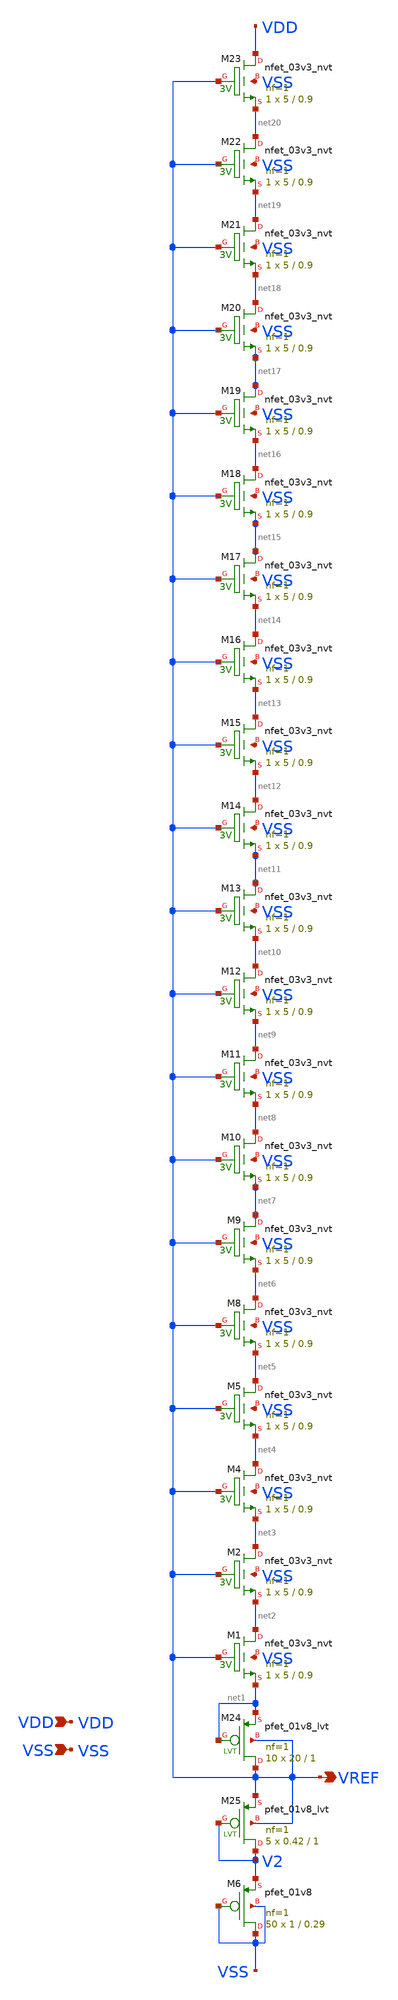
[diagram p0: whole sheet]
** sch_path: design/LELO_SVOD_SKY130A/LELO_SVOD_VTREF.sch
**.subckt LELO_SVOD_VTREF VDD VSS VREF
*.ipin VDD
*.ipin VSS
*.opin VREF
XM1 net2 VREF net1 VSS sky130_fd_pr__nfet_03v3_nvt L=0.9 W=5 nf=1 ad='int((1 + 1)/2) * 5 / 1 * 0.29'
+ as='int((1 + 2)/2) * 5 / 1 * 0.29' pd='2*int((1 + 1)/2) * (5 / 1 + 0.29)' ps='2*int((1 + 2)/2) * (5 / 1 + 0.29)'
+ nrd='0.29 / 5 ' nrs='0.29 / 5 ' sa=0 sb=0 sd=0 mult=1 m=1
XM2 net3 VREF net2 VSS sky130_fd_pr__nfet_03v3_nvt L=0.9 W=5 nf=1 ad='int((1 + 1)/2) * 5 / 1 * 0.29'
+ as='int((1 + 2)/2) * 5 / 1 * 0.29' pd='2*int((1 + 1)/2) * (5 / 1 + 0.29)' ps='2*int((1 + 2)/2) * (5 / 1 + 0.29)'
+ nrd='0.29 / 5 ' nrs='0.29 / 5 ' sa=0 sb=0 sd=0 mult=1 m=1
XM4 net4 VREF net3 VSS sky130_fd_pr__nfet_03v3_nvt L=0.9 W=5 nf=1 ad='int((1 + 1)/2) * 5 / 1 * 0.29'
+ as='int((1 + 2)/2) * 5 / 1 * 0.29' pd='2*int((1 + 1)/2) * (5 / 1 + 0.29)' ps='2*int((1 + 2)/2) * (5 / 1 + 0.29)'
+ nrd='0.29 / 5 ' nrs='0.29 / 5 ' sa=0 sb=0 sd=0 mult=1 m=1
XM5 net5 VREF net4 VSS sky130_fd_pr__nfet_03v3_nvt L=0.9 W=5 nf=1 ad='int((1 + 1)/2) * 5 / 1 * 0.29'
+ as='int((1 + 2)/2) * 5 / 1 * 0.29' pd='2*int((1 + 1)/2) * (5 / 1 + 0.29)' ps='2*int((1 + 2)/2) * (5 / 1 + 0.29)'
+ nrd='0.29 / 5 ' nrs='0.29 / 5 ' sa=0 sb=0 sd=0 mult=1 m=1
XM6 VSS VSS V2 VSS sky130_fd_pr__pfet_01v8 L=0.29 W=1 nf=1 ad='int((1 + 1)/2) * 1 / 1 * 0.29' as='int((1 + 2)/2) * 1 / 1 * 0.29'
+ pd='2*int((1 + 1)/2) * (1 / 1 + 0.29)' ps='2*int((1 + 2)/2) * (1 / 1 + 0.29)' nrd='0.29 / 1 ' nrs='0.29 / 1 '
+ sa=0 sb=0 sd=0 mult=50 m=50
XM8 net6 VREF net5 VSS sky130_fd_pr__nfet_03v3_nvt L=0.9 W=5 nf=1 ad='int((1 + 1)/2) * 5 / 1 * 0.29'
+ as='int((1 + 2)/2) * 5 / 1 * 0.29' pd='2*int((1 + 1)/2) * (5 / 1 + 0.29)' ps='2*int((1 + 2)/2) * (5 / 1 + 0.29)'
+ nrd='0.29 / 5 ' nrs='0.29 / 5 ' sa=0 sb=0 sd=0 mult=1 m=1
XM9 net7 VREF net6 VSS sky130_fd_pr__nfet_03v3_nvt L=0.9 W=5 nf=1 ad='int((1 + 1)/2) * 5 / 1 * 0.29'
+ as='int((1 + 2)/2) * 5 / 1 * 0.29' pd='2*int((1 + 1)/2) * (5 / 1 + 0.29)' ps='2*int((1 + 2)/2) * (5 / 1 + 0.29)'
+ nrd='0.29 / 5 ' nrs='0.29 / 5 ' sa=0 sb=0 sd=0 mult=1 m=1
XM10 net8 VREF net7 VSS sky130_fd_pr__nfet_03v3_nvt L=0.9 W=5 nf=1 ad='int((1 + 1)/2) * 5 / 1 * 0.29'
+ as='int((1 + 2)/2) * 5 / 1 * 0.29' pd='2*int((1 + 1)/2) * (5 / 1 + 0.29)' ps='2*int((1 + 2)/2) * (5 / 1 + 0.29)'
+ nrd='0.29 / 5 ' nrs='0.29 / 5 ' sa=0 sb=0 sd=0 mult=1 m=1
XM11 net9 VREF net8 VSS sky130_fd_pr__nfet_03v3_nvt L=0.9 W=5 nf=1 ad='int((1 + 1)/2) * 5 / 1 * 0.29'
+ as='int((1 + 2)/2) * 5 / 1 * 0.29' pd='2*int((1 + 1)/2) * (5 / 1 + 0.29)' ps='2*int((1 + 2)/2) * (5 / 1 + 0.29)'
+ nrd='0.29 / 5 ' nrs='0.29 / 5 ' sa=0 sb=0 sd=0 mult=1 m=1
XM12 net10 VREF net9 VSS sky130_fd_pr__nfet_03v3_nvt L=0.9 W=5 nf=1 ad='int((1 + 1)/2) * 5 / 1 * 0.29'
+ as='int((1 + 2)/2) * 5 / 1 * 0.29' pd='2*int((1 + 1)/2) * (5 / 1 + 0.29)' ps='2*int((1 + 2)/2) * (5 / 1 + 0.29)'
+ nrd='0.29 / 5 ' nrs='0.29 / 5 ' sa=0 sb=0 sd=0 mult=1 m=1
XM13 net11 VREF net10 VSS sky130_fd_pr__nfet_03v3_nvt L=0.9 W=5 nf=1 ad='int((1 + 1)/2) * 5 / 1 * 0.29'
+ as='int((1 + 2)/2) * 5 / 1 * 0.29' pd='2*int((1 + 1)/2) * (5 / 1 + 0.29)' ps='2*int((1 + 2)/2) * (5 / 1 + 0.29)'
+ nrd='0.29 / 5 ' nrs='0.29 / 5 ' sa=0 sb=0 sd=0 mult=1 m=1
XM14 net12 VREF net11 VSS sky130_fd_pr__nfet_03v3_nvt L=0.9 W=5 nf=1 ad='int((1 + 1)/2) * 5 / 1 * 0.29'
+ as='int((1 + 2)/2) * 5 / 1 * 0.29' pd='2*int((1 + 1)/2) * (5 / 1 + 0.29)' ps='2*int((1 + 2)/2) * (5 / 1 + 0.29)'
+ nrd='0.29 / 5 ' nrs='0.29 / 5 ' sa=0 sb=0 sd=0 mult=1 m=1
XM15 net13 VREF net12 VSS sky130_fd_pr__nfet_03v3_nvt L=0.9 W=5 nf=1 ad='int((1 + 1)/2) * 5 / 1 * 0.29'
+ as='int((1 + 2)/2) * 5 / 1 * 0.29' pd='2*int((1 + 1)/2) * (5 / 1 + 0.29)' ps='2*int((1 + 2)/2) * (5 / 1 + 0.29)'
+ nrd='0.29 / 5 ' nrs='0.29 / 5 ' sa=0 sb=0 sd=0 mult=1 m=1
XM16 net14 VREF net13 VSS sky130_fd_pr__nfet_03v3_nvt L=0.9 W=5 nf=1 ad='int((1 + 1)/2) * 5 / 1 * 0.29'
+ as='int((1 + 2)/2) * 5 / 1 * 0.29' pd='2*int((1 + 1)/2) * (5 / 1 + 0.29)' ps='2*int((1 + 2)/2) * (5 / 1 + 0.29)'
+ nrd='0.29 / 5 ' nrs='0.29 / 5 ' sa=0 sb=0 sd=0 mult=1 m=1
XM17 net15 VREF net14 VSS sky130_fd_pr__nfet_03v3_nvt L=0.9 W=5 nf=1 ad='int((1 + 1)/2) * 5 / 1 * 0.29'
+ as='int((1 + 2)/2) * 5 / 1 * 0.29' pd='2*int((1 + 1)/2) * (5 / 1 + 0.29)' ps='2*int((1 + 2)/2) * (5 / 1 + 0.29)'
+ nrd='0.29 / 5 ' nrs='0.29 / 5 ' sa=0 sb=0 sd=0 mult=1 m=1
XM18 net16 VREF net15 VSS sky130_fd_pr__nfet_03v3_nvt L=0.9 W=5 nf=1 ad='int((1 + 1)/2) * 5 / 1 * 0.29'
+ as='int((1 + 2)/2) * 5 / 1 * 0.29' pd='2*int((1 + 1)/2) * (5 / 1 + 0.29)' ps='2*int((1 + 2)/2) * (5 / 1 + 0.29)'
+ nrd='0.29 / 5 ' nrs='0.29 / 5 ' sa=0 sb=0 sd=0 mult=1 m=1
XM19 net17 VREF net16 VSS sky130_fd_pr__nfet_03v3_nvt L=0.9 W=5 nf=1 ad='int((1 + 1)/2) * 5 / 1 * 0.29'
+ as='int((1 + 2)/2) * 5 / 1 * 0.29' pd='2*int((1 + 1)/2) * (5 / 1 + 0.29)' ps='2*int((1 + 2)/2) * (5 / 1 + 0.29)'
+ nrd='0.29 / 5 ' nrs='0.29 / 5 ' sa=0 sb=0 sd=0 mult=1 m=1
XM20 net18 VREF net17 VSS sky130_fd_pr__nfet_03v3_nvt L=0.9 W=5 nf=1 ad='int((1 + 1)/2) * 5 / 1 * 0.29'
+ as='int((1 + 2)/2) * 5 / 1 * 0.29' pd='2*int((1 + 1)/2) * (5 / 1 + 0.29)' ps='2*int((1 + 2)/2) * (5 / 1 + 0.29)'
+ nrd='0.29 / 5 ' nrs='0.29 / 5 ' sa=0 sb=0 sd=0 mult=1 m=1
XM21 net19 VREF net18 VSS sky130_fd_pr__nfet_03v3_nvt L=0.9 W=5 nf=1 ad='int((1 + 1)/2) * 5 / 1 * 0.29'
+ as='int((1 + 2)/2) * 5 / 1 * 0.29' pd='2*int((1 + 1)/2) * (5 / 1 + 0.29)' ps='2*int((1 + 2)/2) * (5 / 1 + 0.29)'
+ nrd='0.29 / 5 ' nrs='0.29 / 5 ' sa=0 sb=0 sd=0 mult=1 m=1
XM22 net20 VREF net19 VSS sky130_fd_pr__nfet_03v3_nvt L=0.9 W=5 nf=1 ad='int((1 + 1)/2) * 5 / 1 * 0.29'
+ as='int((1 + 2)/2) * 5 / 1 * 0.29' pd='2*int((1 + 1)/2) * (5 / 1 + 0.29)' ps='2*int((1 + 2)/2) * (5 / 1 + 0.29)'
+ nrd='0.29 / 5 ' nrs='0.29 / 5 ' sa=0 sb=0 sd=0 mult=1 m=1
XM23 VDD VREF net20 VSS sky130_fd_pr__nfet_03v3_nvt L=0.9 W=5 nf=1 ad='int((1 + 1)/2) * 5 / 1 * 0.29'
+ as='int((1 + 2)/2) * 5 / 1 * 0.29' pd='2*int((1 + 1)/2) * (5 / 1 + 0.29)' ps='2*int((1 + 2)/2) * (5 / 1 + 0.29)'
+ nrd='0.29 / 5 ' nrs='0.29 / 5 ' sa=0 sb=0 sd=0 mult=1 m=1
XM24 VREF net1 net1 VREF sky130_fd_pr__pfet_01v8_lvt L=1 W=20 nf=1 ad='int((1 + 1)/2) * 20 / 1 * 0.29'
+ as='int((1 + 2)/2) * 20 / 1 * 0.29' pd='2*int((1 + 1)/2) * (20 / 1 + 0.29)' ps='2*int((1 + 2)/2) * (20 / 1 + 0.29)'
+ nrd='0.29 / 20 ' nrs='0.29 / 20 ' sa=0 sb=0 sd=0 mult=10 m=10
XM25 V2 V2 VREF VREF sky130_fd_pr__pfet_01v8_lvt L=1 W=0.42 nf=1 ad='int((1 + 1)/2) * 0.42 / 1 * 0.29'
+ as='int((1 + 2)/2) * 0.42 / 1 * 0.29' pd='2*int((1 + 1)/2) * (0.42 / 1 + 0.29)' ps='2*int((1 + 2)/2) * (0.42 / 1 + 0.29)'
+ nrd='0.29 / 0.42 ' nrs='0.29 / 0.42 ' sa=0 sb=0 sd=0 mult=5 m=5
**.ends
.end
